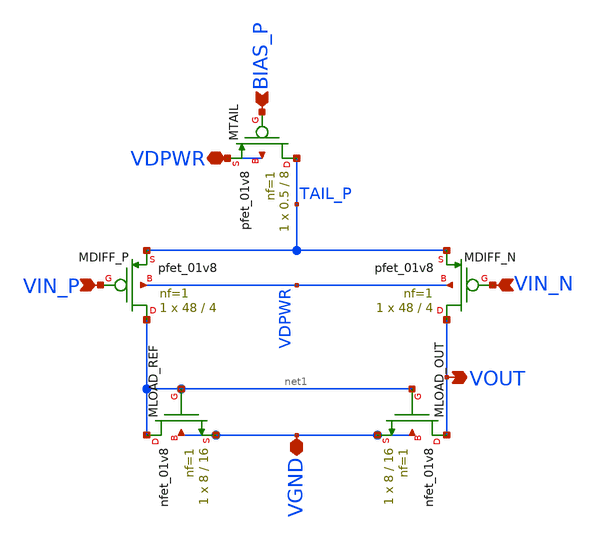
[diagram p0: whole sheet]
** sch_path: xschem-new/ota_5t.sch
**.subckt ota_5t VIN_P VIN_N BIAS_P VDPWR VGND VOUT
*.ipin VIN_P
*.ipin VIN_N
*.ipin BIAS_P
*.iopin VDPWR
*.iopin VGND
*.opin VOUT
XMDIFF_P net1 VIN_P TAIL_P VDPWR sky130_fd_pr__pfet_01v8 L=4 W=48 nf=1 ad='int((1 + 1)/2) * 48 / 1 * 0.29'
+ as='int((1 + 2)/2) * 48 / 1 * 0.29' pd='2*int((1 + 1)/2) * (48 / 1 + 0.29)' ps='2*int((1 + 2)/2) * (48 / 1 + 0.29)'
+ nrd='0.29 / 48 ' nrs='0.29 / 48 ' sa=0 sb=0 sd=0 mult=1 m=1
XMDIFF_N VOUT VIN_N TAIL_P VDPWR sky130_fd_pr__pfet_01v8 L=4 W=48 nf=1 ad='int((1 + 1)/2) * 48 / 1 * 0.29'
+ as='int((1 + 2)/2) * 48 / 1 * 0.29' pd='2*int((1 + 1)/2) * (48 / 1 + 0.29)' ps='2*int((1 + 2)/2) * (48 / 1 + 0.29)'
+ nrd='0.29 / 48 ' nrs='0.29 / 48 ' sa=0 sb=0 sd=0 mult=1 m=1
XMTAIL TAIL_P BIAS_P VDPWR VDPWR sky130_fd_pr__pfet_01v8 L=8 W=0.5 nf=1 ad='int((1 + 1)/2) * 0.5 / 1 * 0.29'
+ as='int((1 + 2)/2) * 0.5 / 1 * 0.29' pd='2*int((1 + 1)/2) * (0.5 / 1 + 0.29)' ps='2*int((1 + 2)/2) * (0.5 / 1 + 0.29)'
+ nrd='0.29 / 0.5 ' nrs='0.29 / 0.5 ' sa=0 sb=0 sd=0 mult=1 m=1
XMLOAD_REF net1 net1 VGND VGND sky130_fd_pr__nfet_01v8 L=16 W=8 nf=1 ad='int((1 + 1)/2) * 8 / 1 * 0.29'
+ as='int((1 + 2)/2) * 8 / 1 * 0.29' pd='2*int((1 + 1)/2) * (8 / 1 + 0.29)' ps='2*int((1 + 2)/2) * (8 / 1 + 0.29)'
+ nrd='0.29 / 8 ' nrs='0.29 / 8 ' sa=0 sb=0 sd=0 mult=1 m=1
XMLOAD_OUT VOUT net1 VGND VGND sky130_fd_pr__nfet_01v8 L=16 W=8 nf=1 ad='int((1 + 1)/2) * 8 / 1 * 0.29'
+ as='int((1 + 2)/2) * 8 / 1 * 0.29' pd='2*int((1 + 1)/2) * (8 / 1 + 0.29)' ps='2*int((1 + 2)/2) * (8 / 1 + 0.29)'
+ nrd='0.29 / 8 ' nrs='0.29 / 8 ' sa=0 sb=0 sd=0 mult=1 m=1
**.ends
.end
